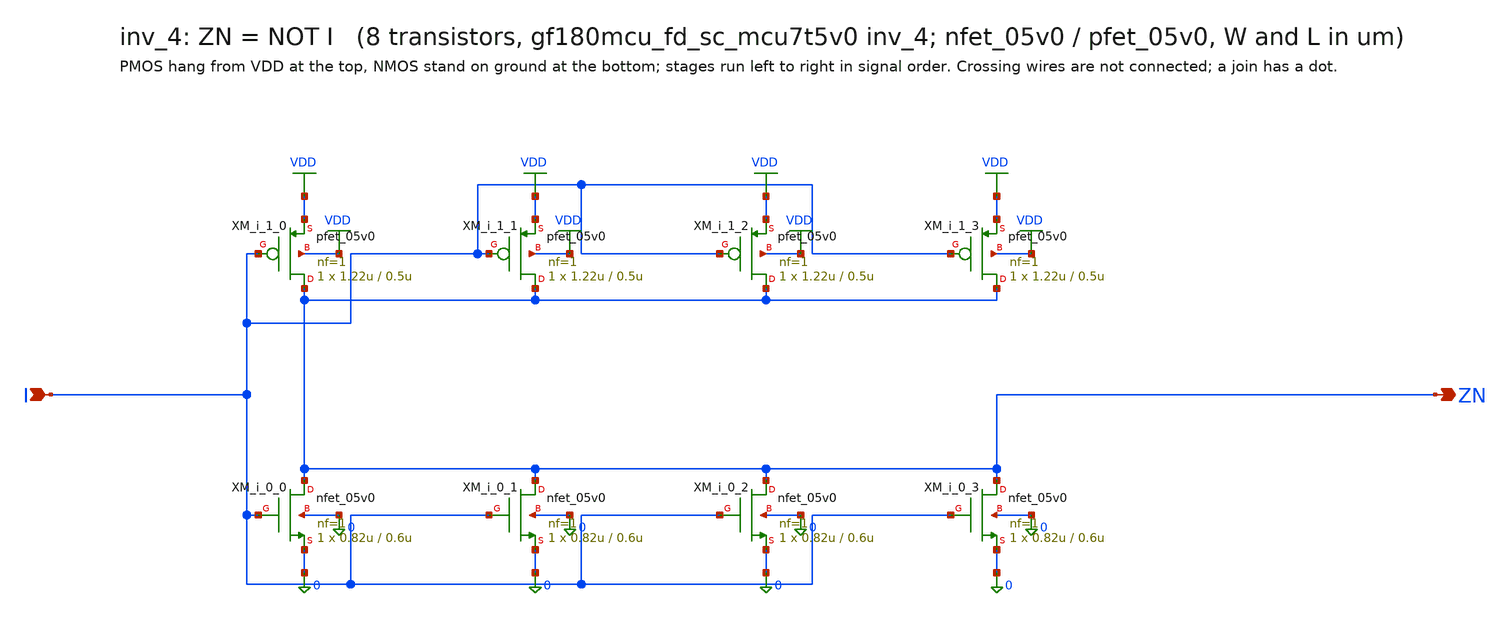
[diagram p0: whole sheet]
** sch_path: xschem/cells_tx/inv_4.sch
**.subckt inv_4 I ZN
*.ipin I
*.opin ZN
XM_i_0_0 ZN I 0 0 nfet_05v0 L=0.6u W=0.82u nf=1 ad=4.1e-13 as=4.1e-13 pd=2.64e-06 ps=2.64e-06 nrd=0
+ nrs=0 sa=0 sb=0 sd=0 m=1
XM_i_0_1 ZN I 0 0 nfet_05v0 L=0.6u W=0.82u nf=1 ad=4.1e-13 as=4.1e-13 pd=2.64e-06 ps=2.64e-06 nrd=0
+ nrs=0 sa=0 sb=0 sd=0 m=1
XM_i_0_2 ZN I 0 0 nfet_05v0 L=0.6u W=0.82u nf=1 ad=4.1e-13 as=4.1e-13 pd=2.64e-06 ps=2.64e-06 nrd=0
+ nrs=0 sa=0 sb=0 sd=0 m=1
XM_i_0_3 ZN I 0 0 nfet_05v0 L=0.6u W=0.82u nf=1 ad=4.1e-13 as=4.1e-13 pd=2.64e-06 ps=2.64e-06 nrd=0
+ nrs=0 sa=0 sb=0 sd=0 m=1
XM_i_1_0 ZN I VDD VDD pfet_05v0 L=0.5u W=1.22u nf=1 ad=6.1e-13 as=6.1e-13 pd=3.44e-06 ps=3.44e-06
+ nrd=0 nrs=0 sa=0 sb=0 sd=0 m=1
XM_i_1_1 ZN I VDD VDD pfet_05v0 L=0.5u W=1.22u nf=1 ad=6.1e-13 as=6.1e-13 pd=3.44e-06 ps=3.44e-06
+ nrd=0 nrs=0 sa=0 sb=0 sd=0 m=1
XM_i_1_2 ZN I VDD VDD pfet_05v0 L=0.5u W=1.22u nf=1 ad=6.1e-13 as=6.1e-13 pd=3.44e-06 ps=3.44e-06
+ nrd=0 nrs=0 sa=0 sb=0 sd=0 m=1
XM_i_1_3 ZN I VDD VDD pfet_05v0 L=0.5u W=1.22u nf=1 ad=6.1e-13 as=6.1e-13 pd=3.44e-06 ps=3.44e-06
+ nrd=0 nrs=0 sa=0 sb=0 sd=0 m=1
**.ends
.GLOBAL VDD
.end
